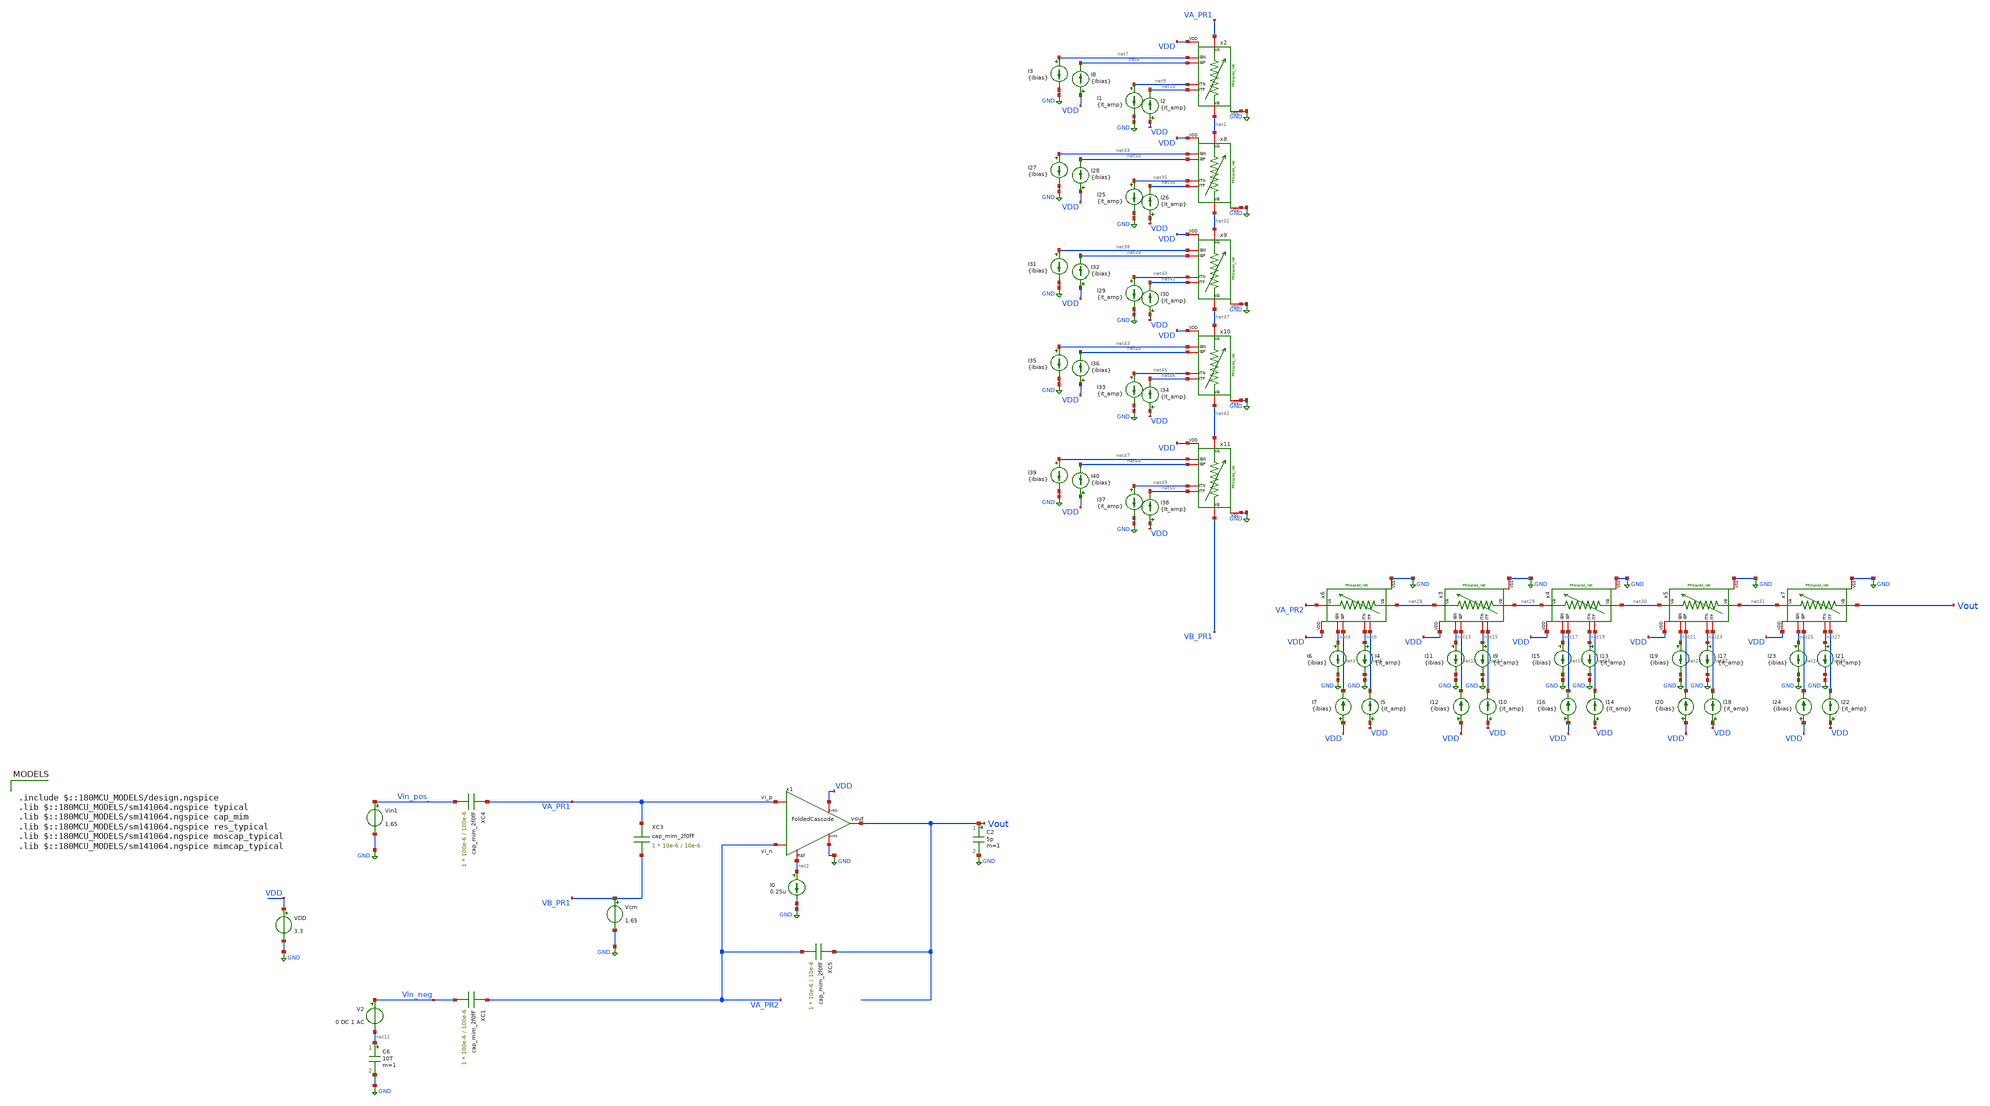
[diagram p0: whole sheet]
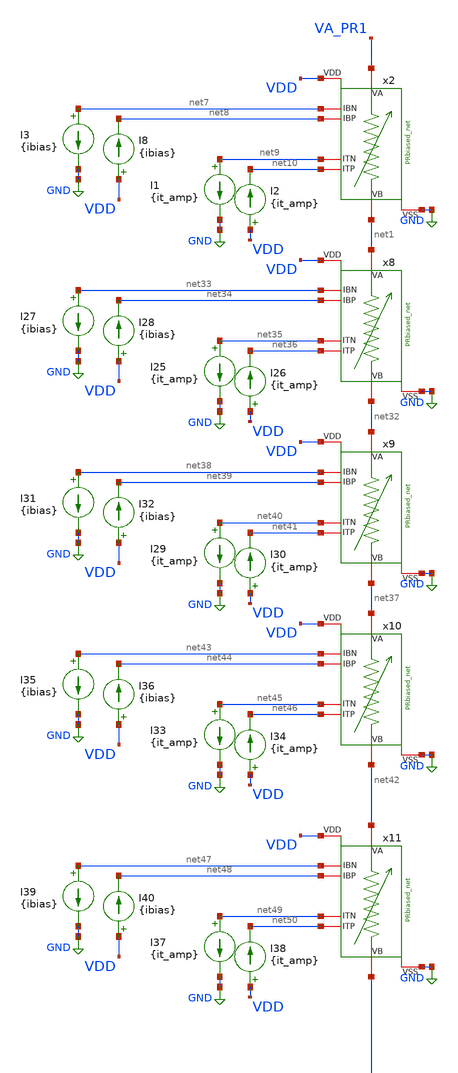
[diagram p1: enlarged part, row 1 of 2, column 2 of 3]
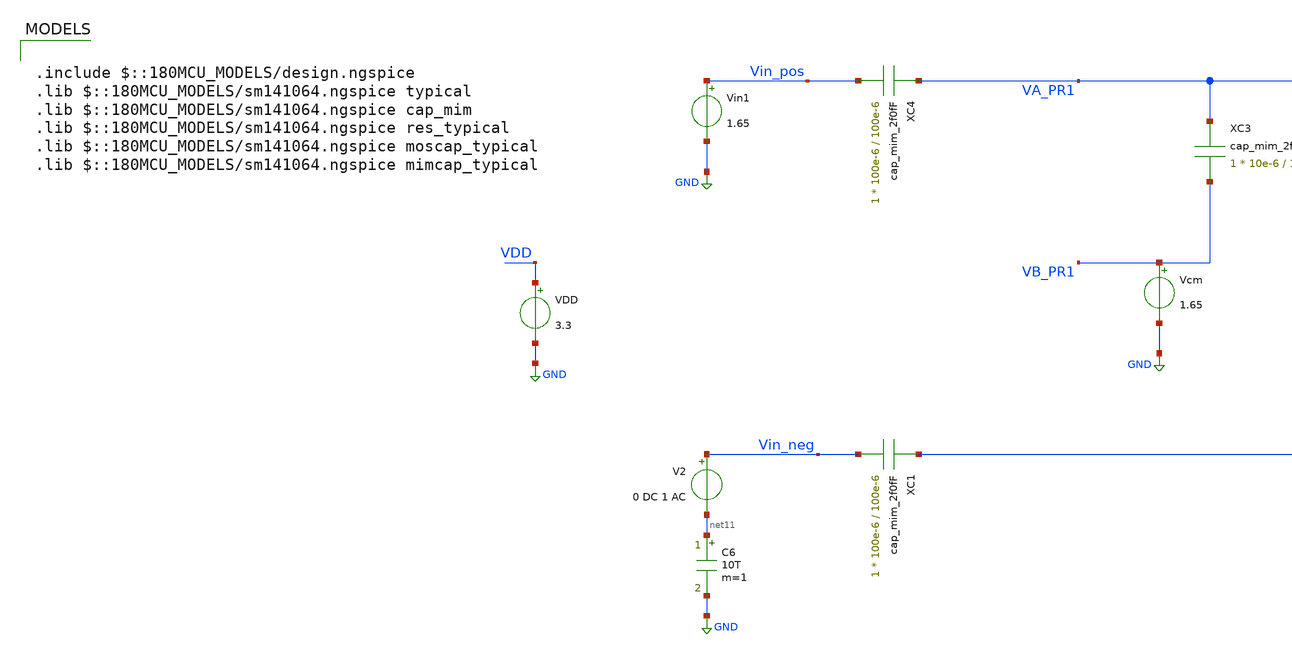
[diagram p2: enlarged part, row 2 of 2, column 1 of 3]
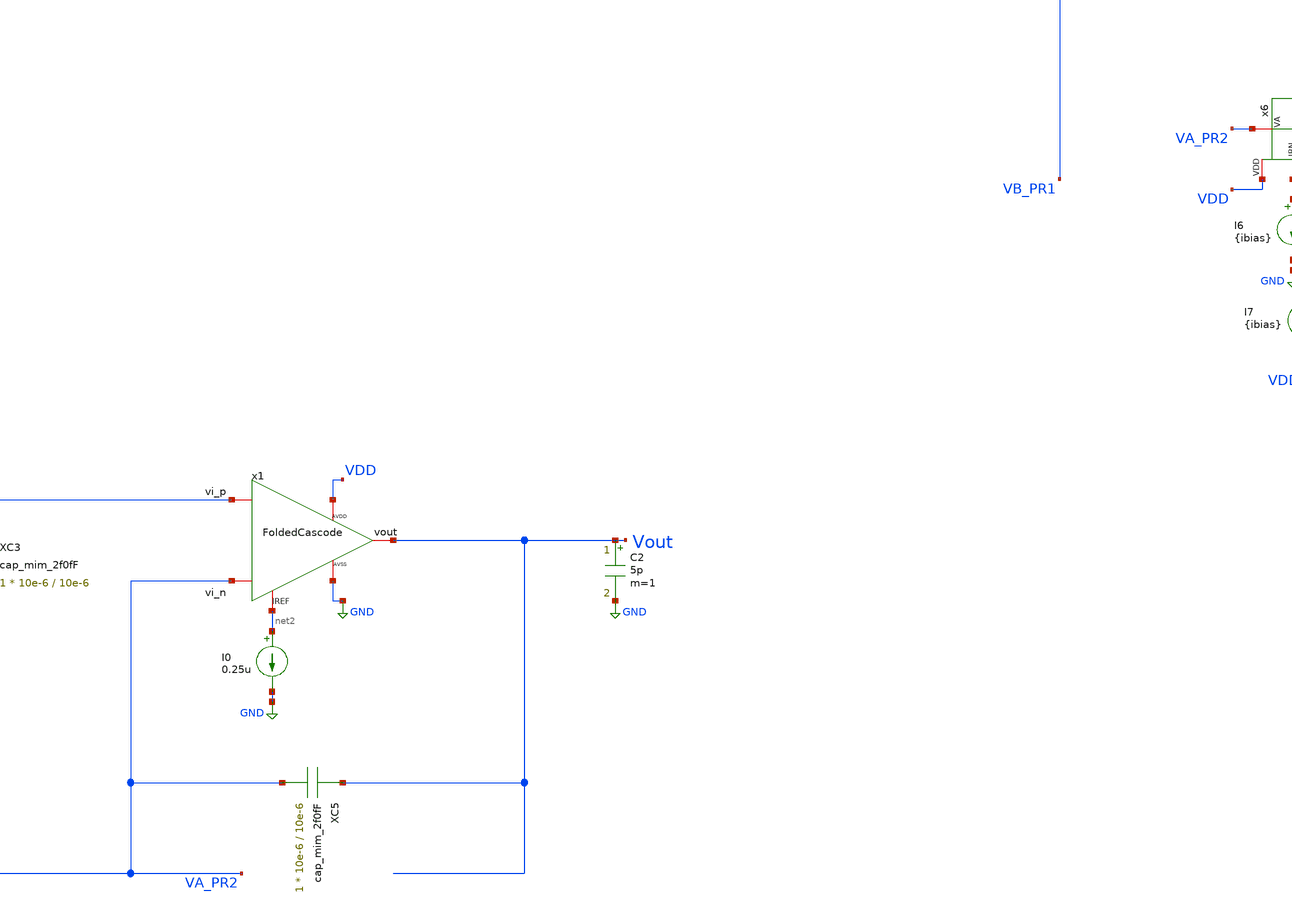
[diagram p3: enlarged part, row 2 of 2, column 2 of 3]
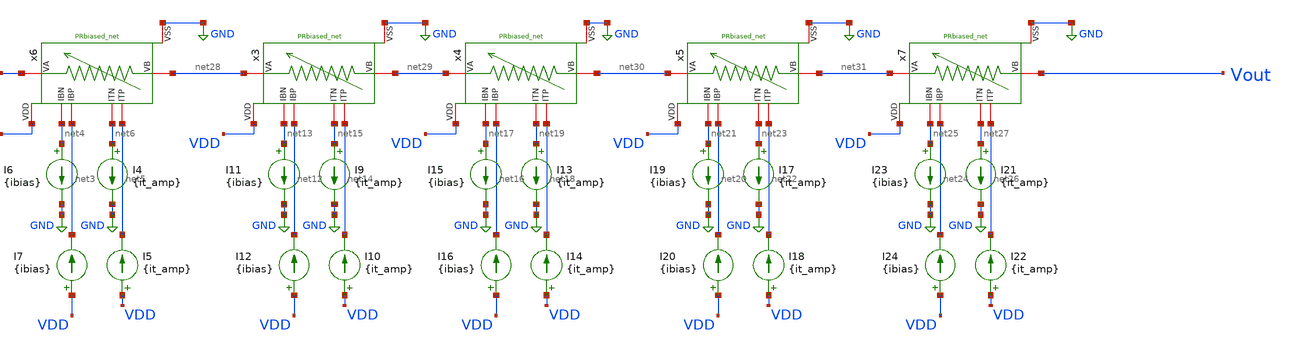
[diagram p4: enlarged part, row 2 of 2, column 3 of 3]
** sch_path: TIA/TB_filter_ac.sch
**.subckt TB_filter_ac
VDD VDD GND 3.3
C2 Vout GND 5p m=1
x1 VA_PR1 VA_PR2 Vout net2 VDD GND FoldedCascode
x6 VA_PR2 net28 net4 net3 net6 net5 VDD GND PRbiased_net
x2 VA_PR1 net1 net7 net8 net9 net10 VDD GND PRbiased_net
I0 net2 GND 0.25u
I4 net6 GND {it_amp}
I5 VDD net5 {it_amp}
I6 net4 GND {ibias}
I7 VDD net3 {ibias}
Vcm VB_PR1 GND 1.65
I1 net9 GND {it_amp}
I2 VDD net10 {it_amp}
I3 net7 GND {ibias}
I8 VDD net8 {ibias}
Vin1 Vin_pos GND 1.65
V2 Vin_neg net11 0 DC 1 AC
C6 net11 GND 10T m=1
x3 net28 net29 net13 net12 net15 net14 VDD GND PRbiased_net
I9 net15 GND {it_amp}
I10 VDD net14 {it_amp}
I11 net13 GND {ibias}
I12 VDD net12 {ibias}
x4 net29 net30 net17 net16 net19 net18 VDD GND PRbiased_net
I13 net19 GND {it_amp}
I14 VDD net18 {it_amp}
I15 net17 GND {ibias}
I16 VDD net16 {ibias}
x5 net30 net31 net21 net20 net23 net22 VDD GND PRbiased_net
I17 net23 GND {it_amp}
I18 VDD net22 {it_amp}
I19 net21 GND {ibias}
I20 VDD net20 {ibias}
x7 net31 Vout net25 net24 net27 net26 VDD GND PRbiased_net
I21 net27 GND {it_amp}
I22 VDD net26 {it_amp}
I23 net25 GND {ibias}
I24 VDD net24 {ibias}
x8 net1 net32 net33 net34 net35 net36 VDD GND PRbiased_net
I25 net35 GND {it_amp}
I26 VDD net36 {it_amp}
I27 net33 GND {ibias}
I28 VDD net34 {ibias}
x9 net32 net37 net38 net39 net40 net41 VDD GND PRbiased_net
I29 net40 GND {it_amp}
I30 VDD net41 {it_amp}
I31 net38 GND {ibias}
I32 VDD net39 {ibias}
x10 net37 net42 net43 net44 net45 net46 VDD GND PRbiased_net
I33 net45 GND {it_amp}
I34 VDD net46 {it_amp}
I35 net43 GND {ibias}
I36 VDD net44 {ibias}
x11 net42 VB_PR1 net47 net48 net49 net50 VDD GND PRbiased_net
I37 net49 GND {it_amp}
I38 VDD net50 {it_amp}
I39 net47 GND {ibias}
I40 VDD net48 {ibias}
XC4 VA_PR1 Vin_pos cap_mim_2f0fF c_width=100e-6 c_length=100e-6 m=1
XC1 VA_PR2 Vin_neg cap_mim_2f0fF c_width=100e-6 c_length=100e-6 m=1
XC3 VA_PR1 VB_PR1 cap_mim_2f0fF c_width=10e-6 c_length=10e-6 m=1
XC5 Vout VA_PR2 cap_mim_2f0fF c_width=10e-6 c_length=10e-6 m=1
**** begin user architecture code

.include $::180MCU_MODELS/design.ngspice
.lib $::180MCU_MODELS/sm141064.ngspice typical
.lib $::180MCU_MODELS/sm141064.ngspice cap_mim
.lib $::180MCU_MODELS/sm141064.ngspice res_typical
.lib $::180MCU_MODELS/sm141064.ngspice moscap_typical
.lib $::180MCU_MODELS/sm141064.ngspice mimcap_typical



.option gmin=1e-16
.OPTION ABSTOL=1e-2

*.nodeset v(Vin_neg)=1.65
*.nodeset v(vout)=1.65

.nodeset all=1.65

.param ibias = 1p
.param it_amp = 2p

.control
save all

let sample_index = -27

*tran 10u 10m
*remzerovec
*write TB_TIA_ac.raw
*set appendwrite

*op
*remzerovec
*write TB_filter_ac.raw
*set appendwrite

while sample_index < 110
reset
set temp = $&sample_index

ac dec 10 1m 1e8
remzerovec
write TB_filter_ac.raw
set appendwrite

let sample_index = sample_index + 27
end


.endc
.save all


**** end user architecture code
**.ends
.GLOBAL GND
.end
